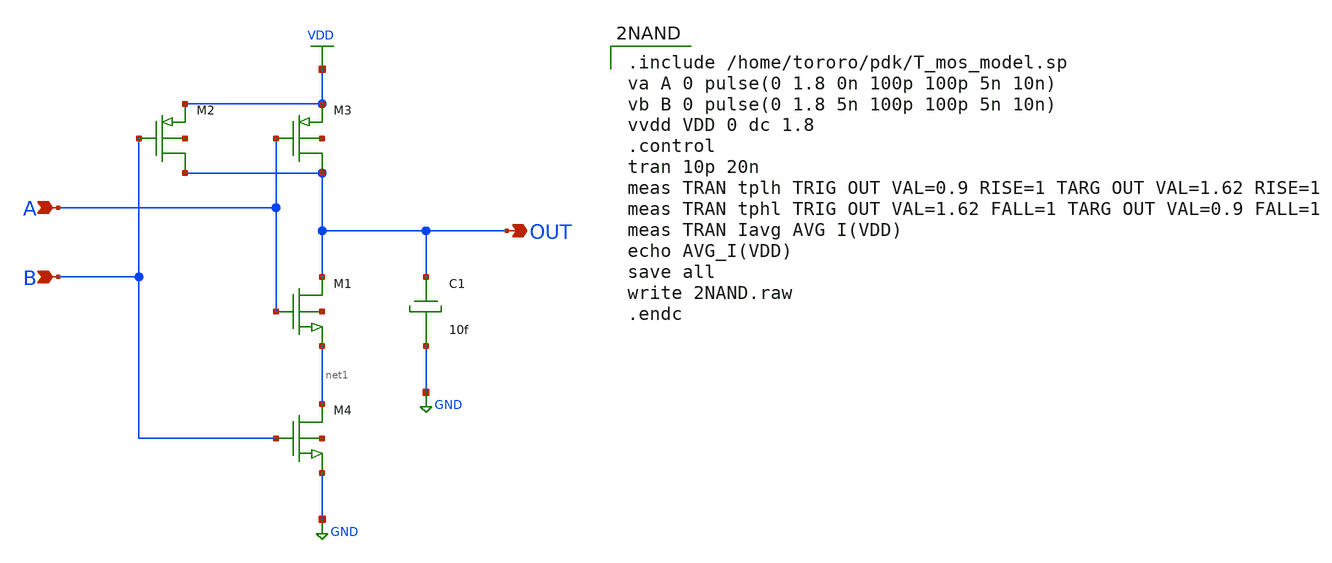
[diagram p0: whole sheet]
** sch_path: task1/2NAND.sch
**.subckt 2NAND OUT B A
*.opin OUT
*.ipin B
*.ipin A
M1 OUT A net1 net2 nch w=9.7u l=1.94u as=0 ps=0 ad=0 pd=0 m=1
M2 OUT B VDD net3 pch w=9.7u l=0.35u as=0 ps=0 ad=0 pd=0 m=1
M3 OUT A VDD net4 pch w=9.7u l=0.35u as=0 ps=0 ad=0 pd=0 m=1
M4 net1 B GND net5 nch w=9.7u l=1.94u as=0 ps=0 ad=0 pd=0 m=1
C1 OUT GND 10f m=1
**** begin user architecture code

.include /home/tororo/pdk/T_mos_model.sp
va A 0 pulse(0 1.8 0n 100p 100p 5n 10n)
vb B 0 pulse(0 1.8 5n 100p 100p 5n 10n)
vvdd VDD 0 dc 1.8
.control
tran 10p 20n
meas TRAN tplh TRIG OUT VAL=0.9 RISE=1 TARG OUT VAL=1.62 RISE=1
meas TRAN tphl TRIG OUT VAL=1.62 FALL=1 TARG OUT VAL=0.9 FALL=1
meas TRAN Iavg AVG I(VDD)
echo AVG_I(VDD)
save all
write 2NAND.raw
.endc

**** end user architecture code
**.ends
.GLOBAL VDD
.GLOBAL GND
.end
